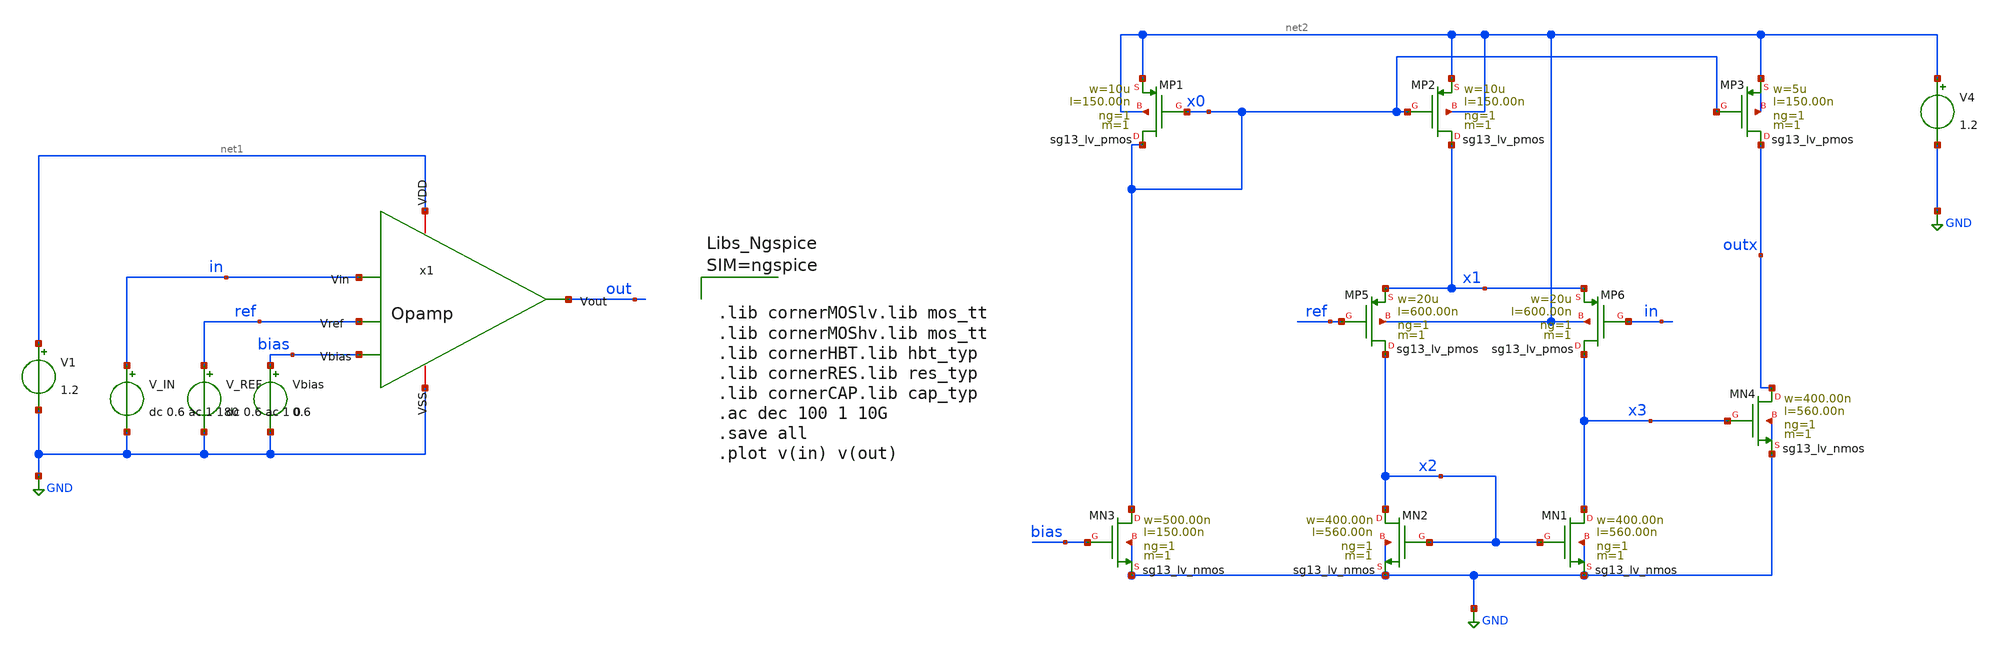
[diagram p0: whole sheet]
** sch_path: netlist/opamptbAC.sch
**.subckt opamptbAC
x1 net1 in ref out bias GND Opamp
V1 net1 GND 1.2
V_REF ref GND dc 0.6 ac 1 0
V_IN in GND dc 0.6 ac 1 180
Vbias bias GND 0.6
XMP1 x0 x0 net2 net2 sg13_lv_pmos w=10u l=150.00n ng=1 m=1 mm_ok=1
XMP2 x1 x0 net2 net2 sg13_lv_pmos w=10u l=150.00n ng=1 m=1 mm_ok=1
XMN1 x3 x2 GND GND sg13_lv_nmos w=400.00n l=560.00n ng=1 m=1 mm_ok=1
XMN2 x2 x2 GND GND sg13_lv_nmos w=400.00n l=560.00n ng=1 m=1 mm_ok=1
XMN3 x0 bias GND GND sg13_lv_nmos w=500.00n l=150.00n ng=1 m=1 mm_ok=1
XMP5 x2 ref x1 net2 sg13_lv_pmos w=20u l=600.00n ng=1 m=1 mm_ok=1
XMP6 x3 in x1 net2 sg13_lv_pmos w=20u l=600.00n ng=1 m=1 mm_ok=1
V4 net2 GND 1.2
XMN4 outx x3 GND GND sg13_lv_nmos w=400.00n l=560.00n ng=1 m=1 mm_ok=1
XMP3 outx x0 net2 net2 sg13_lv_pmos w=5u l=150.00n ng=1 m=1 mm_ok=1
**** begin user architecture code



.lib cornerMOSlv.lib mos_tt
.lib cornerMOShv.lib mos_tt
.lib cornerHBT.lib hbt_typ
.lib cornerRES.lib res_typ
.lib cornerCAP.lib cap_typ
.ac dec 100 1 10G
.save all
.plot v(in) v(out)



**** end user architecture code
**.ends

* expanding   symbol:  Opamp.sym # of pins=6
** sym_path: schematic/Opamp.sym
** sch_path: schematic/Opamp.sch
.subckt Opamp VDD Vin Vref Vout Vbias VSS
*.ipin Vin
*.iopin VDD
*.iopin VSS
*.ipin Vref
*.opin Vout
*.ipin Vbias
XMP5 net4 net4 VDD VDD sg13_lv_pmos w=10u l=150.00n ng=1 m=1 mm_ok=1
XMP6 net1 net4 VDD VDD sg13_lv_pmos w=10u l=150.00n ng=1 m=1 mm_ok=1
XMN4 net3 net2 VSS VSS sg13_lv_nmos w=420.00n l=560.00n ng=1 m=1 mm_ok=1
XMN5 net2 net2 VSS VSS sg13_lv_nmos w=420.00n l=560.00n ng=1 m=1 mm_ok=1
XMN6 net4 Vbias VSS VSS sg13_lv_nmos w=500.00n l=150.00n ng=1 m=1 mm_ok=1
XMP7 net2 Vref net1 VDD sg13_lv_pmos w=10u l=300.00n ng=1 m=1 mm_ok=1
XMP8 net3 Vin net1 VDD sg13_lv_pmos w=10u l=300.00n ng=1 m=1 mm_ok=1
XMN7 Vout net3 VSS VSS sg13_lv_nmos w=420.00n l=560.00n ng=1 m=1 mm_ok=1
XMP9 Vout net4 VDD VDD sg13_lv_pmos w=5u l=150.00n ng=1 m=1 mm_ok=1
.ends

.GLOBAL GND
.end
